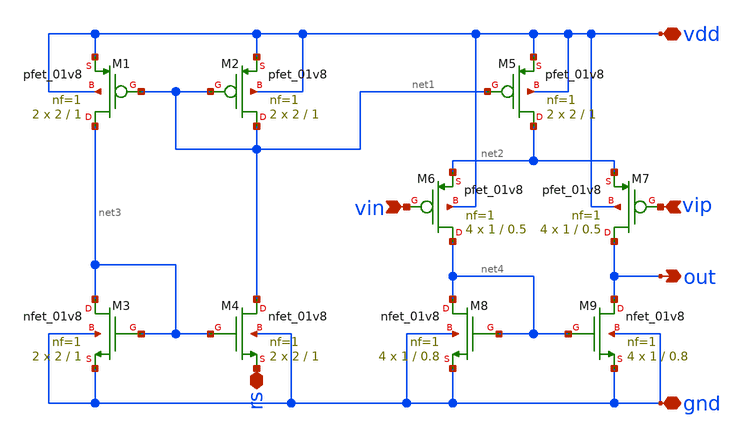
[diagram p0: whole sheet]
** sch_path: OP_Amp/xschem/opamp.sch
**.subckt opamp vdd gnd rs vip vin out
*.iopin vdd
*.iopin gnd
*.iopin rs
*.ipin vip
*.ipin vin
*.opin out
XM3 net3 net3 gnd gnd sky130_fd_pr__nfet_01v8 L=1 W=2 nf=1 ad='int((nf+1)/2) * W/nf * 0.29' as='int((nf+2)/2) * W/nf * 0.29'
+ pd='2*int((nf+1)/2) * (W/nf + 0.29)' ps='2*int((nf+2)/2) * (W/nf + 0.29)' nrd='0.29 / W' nrs='0.29 / W'
+ sa=0 sb=0 sd=0 mult=2 m=2
XM8 net4 net4 gnd gnd sky130_fd_pr__nfet_01v8 L=0.8 W=1 nf=1 ad='int((nf+1)/2) * W/nf * 0.29' as='int((nf+2)/2) * W/nf * 0.29'
+ pd='2*int((nf+1)/2) * (W/nf + 0.29)' ps='2*int((nf+2)/2) * (W/nf + 0.29)' nrd='0.29 / W' nrs='0.29 / W'
+ sa=0 sb=0 sd=0 mult=4 m=4
XM4 net1 net3 rs gnd sky130_fd_pr__nfet_01v8 L=1 W=2 nf=1 ad='int((nf+1)/2) * W/nf * 0.29' as='int((nf+2)/2) * W/nf * 0.29'
+ pd='2*int((nf+1)/2) * (W/nf + 0.29)' ps='2*int((nf+2)/2) * (W/nf + 0.29)' nrd='0.29 / W' nrs='0.29 / W'
+ sa=0 sb=0 sd=0 mult=2 m=2
XM9 out net4 gnd gnd sky130_fd_pr__nfet_01v8 L=0.8 W=1 nf=1 ad='int((nf+1)/2) * W/nf * 0.29' as='int((nf+2)/2) * W/nf * 0.29'
+ pd='2*int((nf+1)/2) * (W/nf + 0.29)' ps='2*int((nf+2)/2) * (W/nf + 0.29)' nrd='0.29 / W' nrs='0.29 / W'
+ sa=0 sb=0 sd=0 mult=4 m=4
XM1 net3 net1 vdd vdd sky130_fd_pr__pfet_01v8 L=1 W=2 nf=1 ad='int((nf+1)/2) * W/nf * 0.29' as='int((nf+2)/2) * W/nf * 0.29'
+ pd='2*int((nf+1)/2) * (W/nf + 0.29)' ps='2*int((nf+2)/2) * (W/nf + 0.29)' nrd='0.29 / W' nrs='0.29 / W'
+ sa=0 sb=0 sd=0 mult=2 m=2
XM2 net1 net1 vdd vdd sky130_fd_pr__pfet_01v8 L=1 W=2 nf=1 ad='int((nf+1)/2) * W/nf * 0.29' as='int((nf+2)/2) * W/nf * 0.29'
+ pd='2*int((nf+1)/2) * (W/nf + 0.29)' ps='2*int((nf+2)/2) * (W/nf + 0.29)' nrd='0.29 / W' nrs='0.29 / W'
+ sa=0 sb=0 sd=0 mult=2 m=2
XM5 net2 net1 vdd vdd sky130_fd_pr__pfet_01v8 L=1 W=2 nf=1 ad='int((nf+1)/2) * W/nf * 0.29' as='int((nf+2)/2) * W/nf * 0.29'
+ pd='2*int((nf+1)/2) * (W/nf + 0.29)' ps='2*int((nf+2)/2) * (W/nf + 0.29)' nrd='0.29 / W' nrs='0.29 / W'
+ sa=0 sb=0 sd=0 mult=2 m=2
XM6 net4 vin net2 vdd sky130_fd_pr__pfet_01v8 L=0.5 W=1 nf=1 ad='int((nf+1)/2) * W/nf * 0.29' as='int((nf+2)/2) * W/nf * 0.29'
+ pd='2*int((nf+1)/2) * (W/nf + 0.29)' ps='2*int((nf+2)/2) * (W/nf + 0.29)' nrd='0.29 / W' nrs='0.29 / W'
+ sa=0 sb=0 sd=0 mult=4 m=4
XM7 out vip net2 vdd sky130_fd_pr__pfet_01v8 L=0.5 W=1 nf=1 ad='int((nf+1)/2) * W/nf * 0.29' as='int((nf+2)/2) * W/nf * 0.29'
+ pd='2*int((nf+1)/2) * (W/nf + 0.29)' ps='2*int((nf+2)/2) * (W/nf + 0.29)' nrd='0.29 / W' nrs='0.29 / W'
+ sa=0 sb=0 sd=0 mult=4 m=4
**.ends
.end
